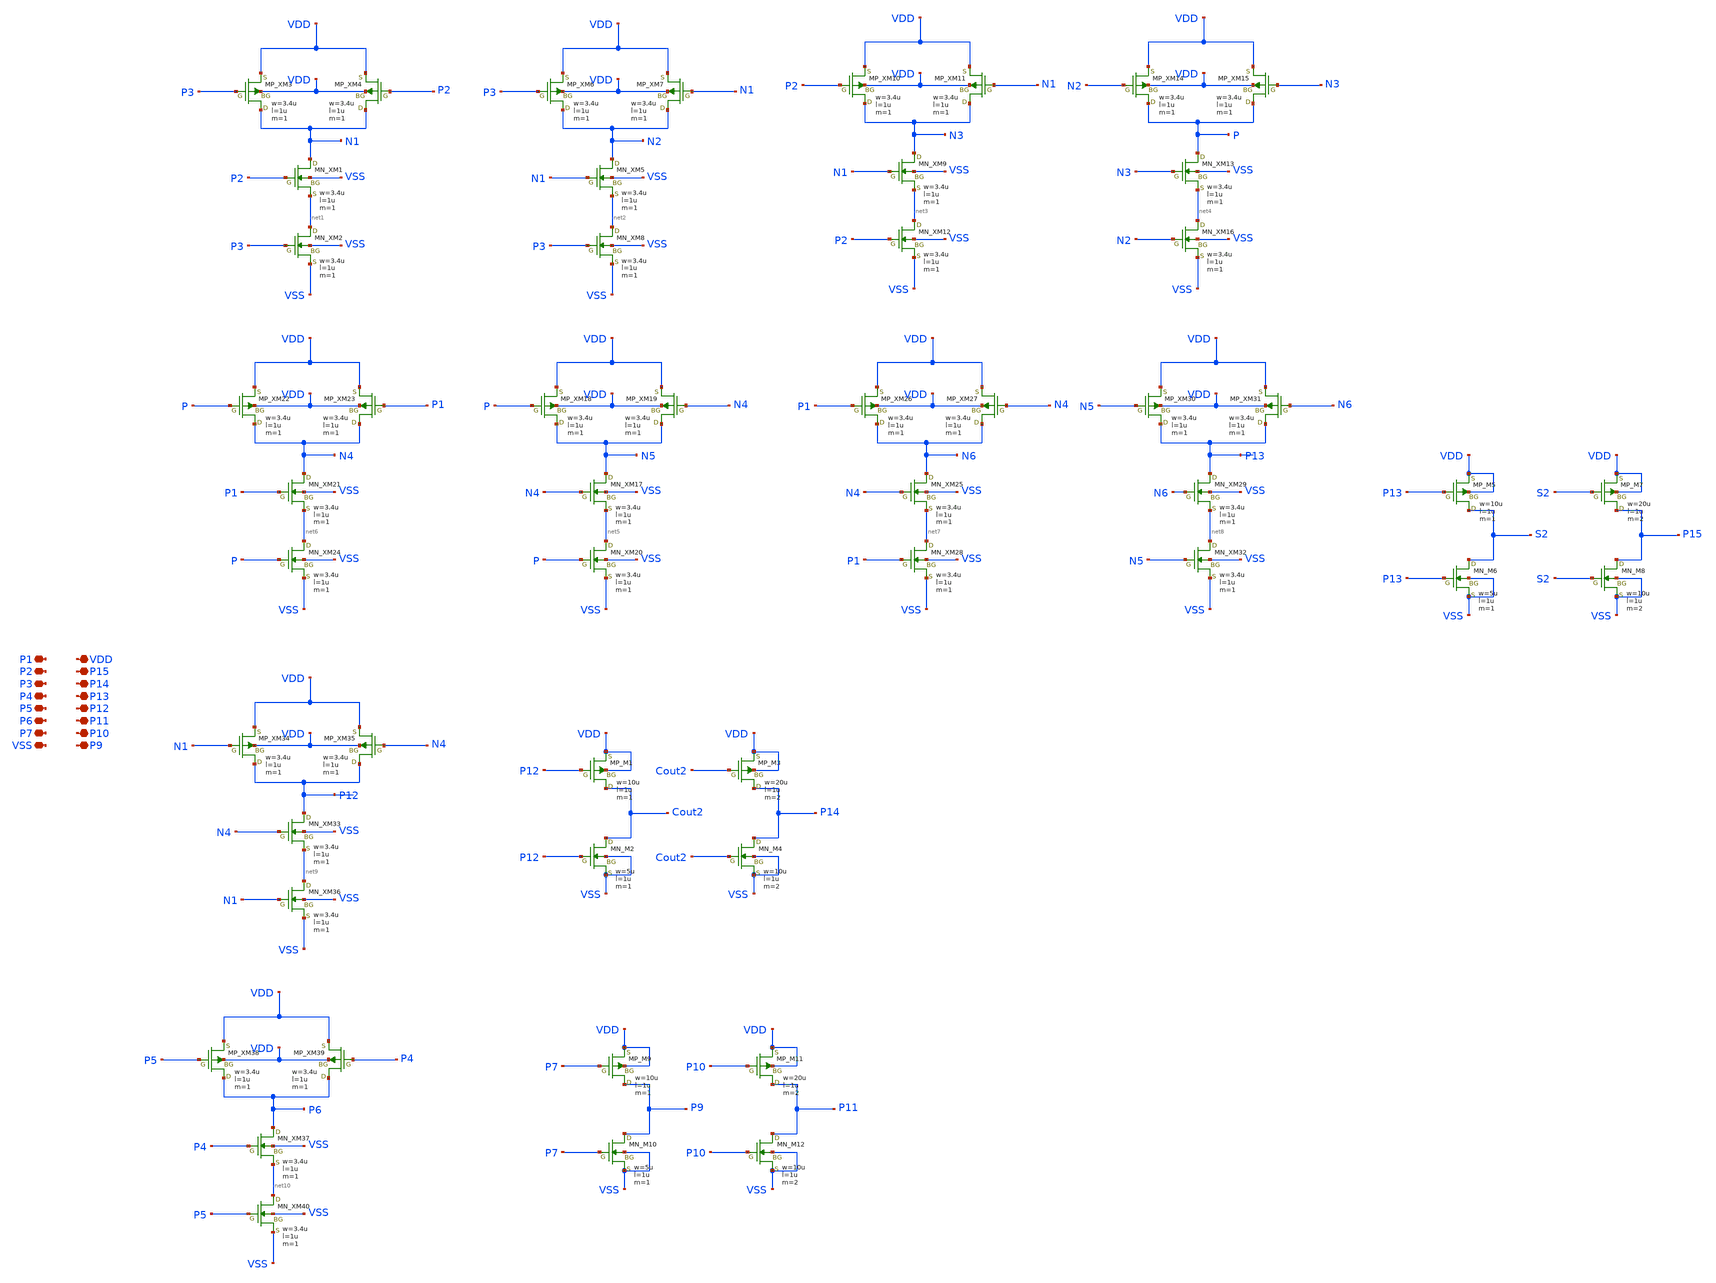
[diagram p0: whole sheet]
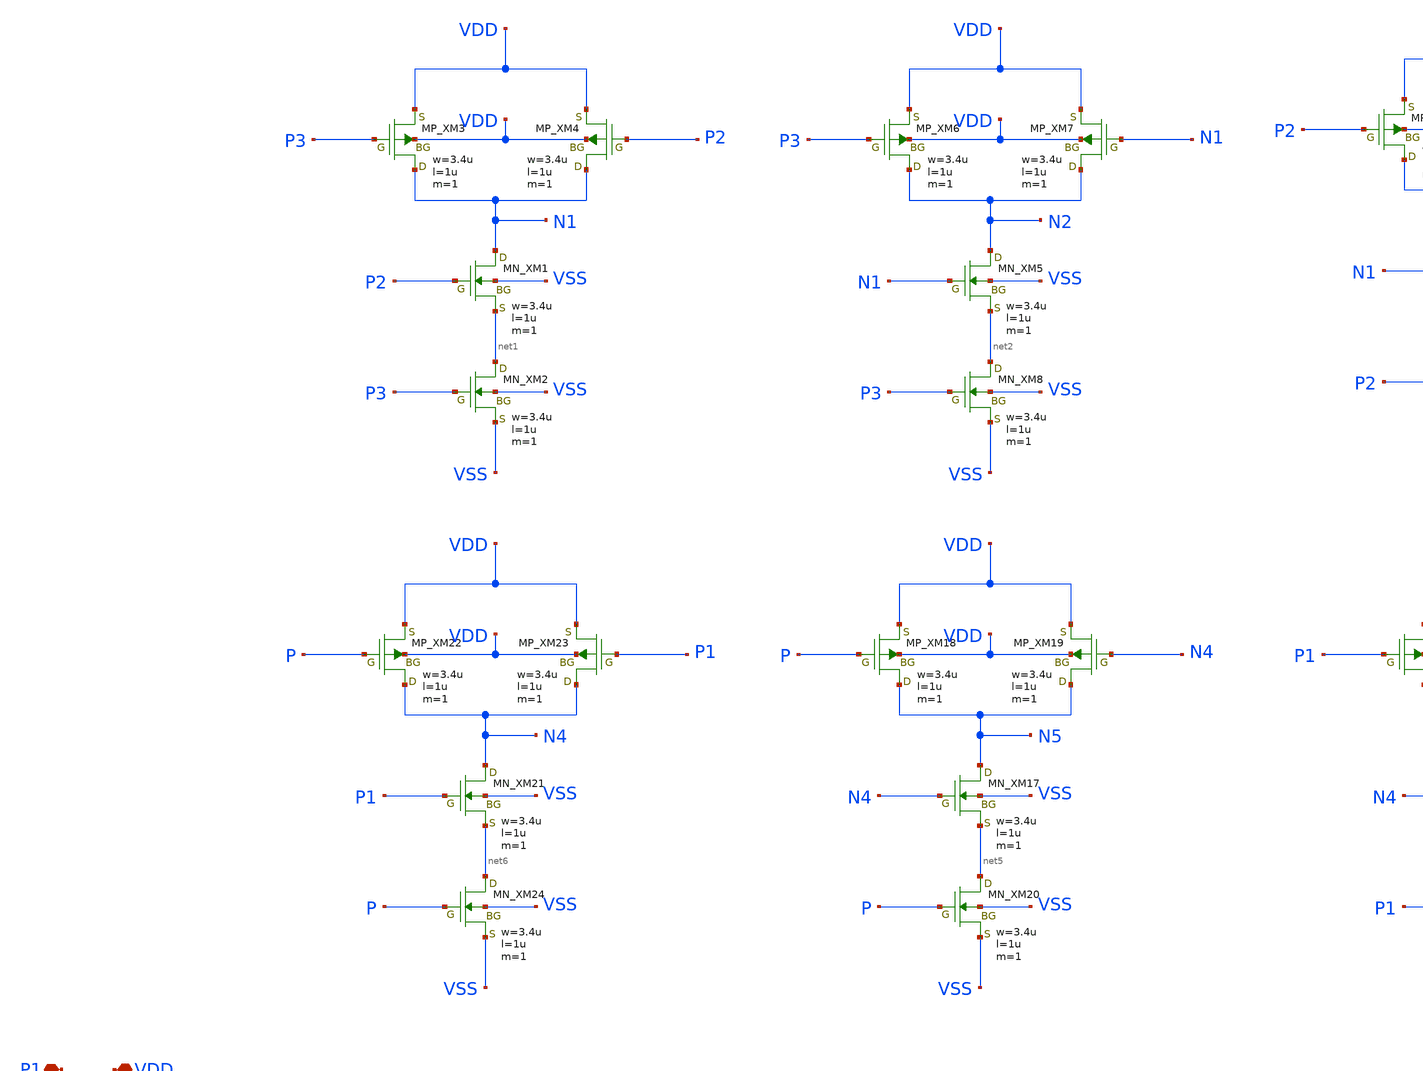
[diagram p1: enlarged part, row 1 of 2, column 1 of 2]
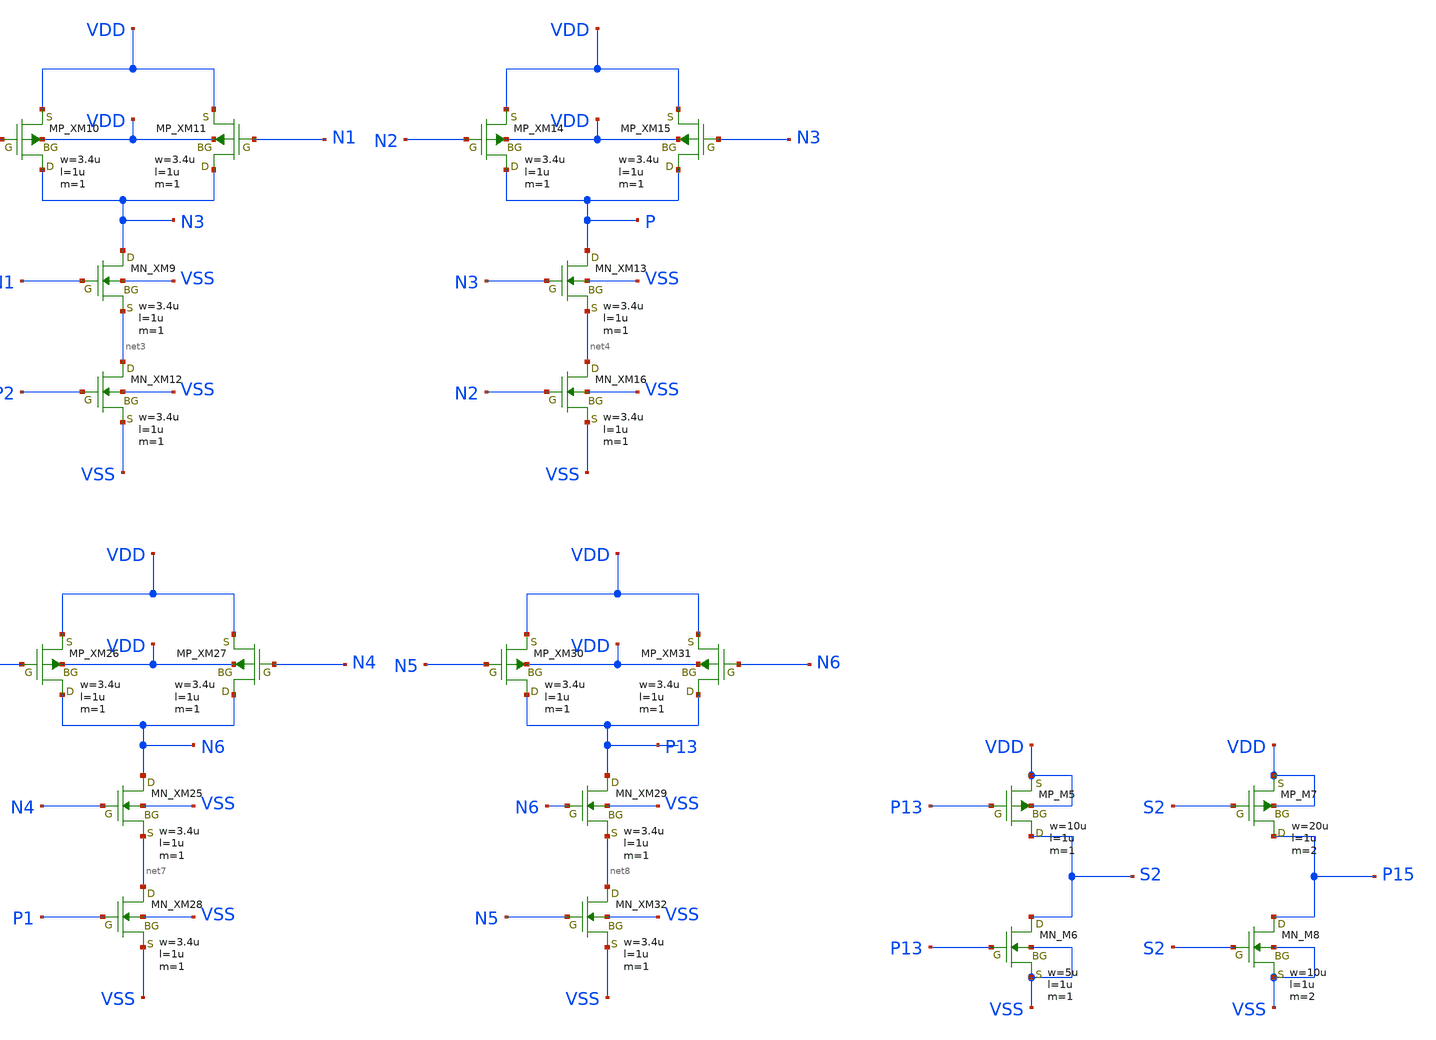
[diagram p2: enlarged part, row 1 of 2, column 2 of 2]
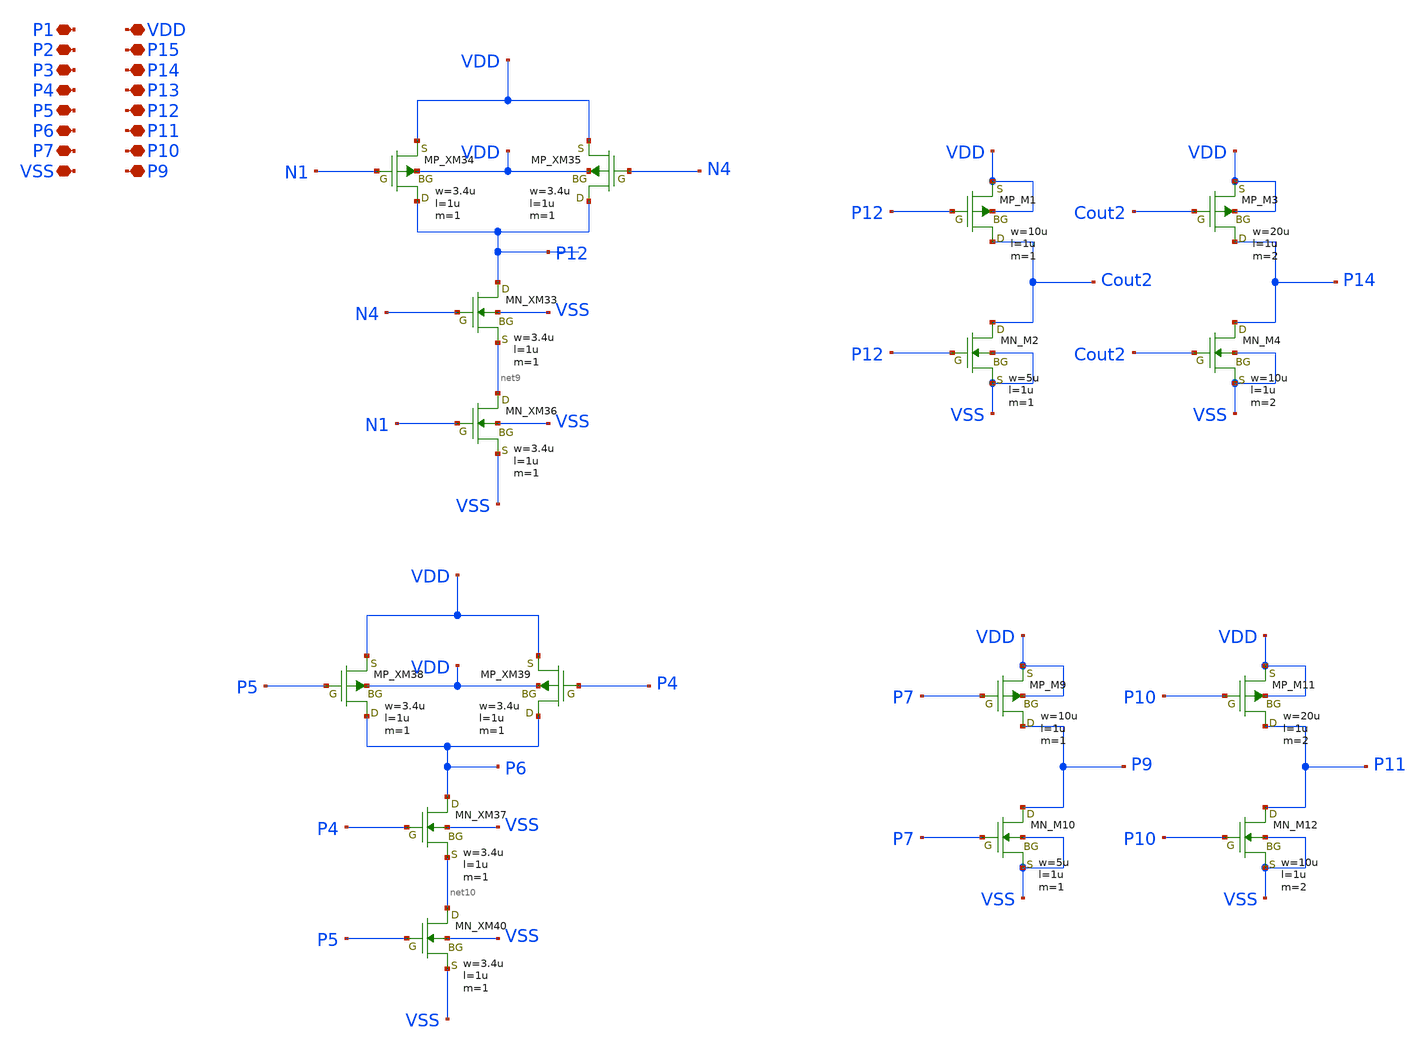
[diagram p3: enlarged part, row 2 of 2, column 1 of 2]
** sch_path: src/tr_1um_AriyoshiNaoki1016jp_bufferadd_ver2.sch
**.subckt tr_1um_AriyoshiNaoki1016jp_bufferadd_ver2 P1 P2 P3 P4 P5 P6 P7 VSS VDD P15 P14 P13 P12 P11
*+ P10 P9
*.iopin P1
*.iopin P2
*.iopin P3
*.iopin P4
*.iopin P5
*.iopin P6
*.iopin P7
*.iopin VSS
*.iopin VDD
*.iopin P15
*.iopin P14
*.iopin P13
*.iopin P12
*.iopin P11
*.iopin P10
*.iopin P9
XXM1 N1 P2 net1 VSS NMOS w=3.4u l=1u nrd=0 nrs=0 m=1
XXM3 N1 P3 VDD VDD PMOS w=3.4u l=1u nrd=0 nrs=0 m=1
XXM4 N1 P2 VDD VDD PMOS w=3.4u l=1u nrd=0 nrs=0 m=1
XXM2 net1 P3 VSS VSS NMOS w=3.4u l=1u nrd=0 nrs=0 m=1
XXM5 N2 N1 net2 VSS NMOS w=3.4u l=1u nrd=0 nrs=0 m=1
XXM6 N2 P3 VDD VDD PMOS w=3.4u l=1u nrd=0 nrs=0 m=1
XXM7 N2 N1 VDD VDD PMOS w=3.4u l=1u nrd=0 nrs=0 m=1
XXM8 net2 P3 VSS VSS NMOS w=3.4u l=1u nrd=0 nrs=0 m=1
XXM9 N3 N1 net3 VSS NMOS w=3.4u l=1u nrd=0 nrs=0 m=1
XXM10 N3 P2 VDD VDD PMOS w=3.4u l=1u nrd=0 nrs=0 m=1
XXM11 N3 N1 VDD VDD PMOS w=3.4u l=1u nrd=0 nrs=0 m=1
XXM12 net3 P2 VSS VSS NMOS w=3.4u l=1u nrd=0 nrs=0 m=1
XXM13 P N3 net4 VSS NMOS w=3.4u l=1u nrd=0 nrs=0 m=1
XXM14 P N2 VDD VDD PMOS w=3.4u l=1u nrd=0 nrs=0 m=1
XXM15 P N3 VDD VDD PMOS w=3.4u l=1u nrd=0 nrs=0 m=1
XXM16 net4 N2 VSS VSS NMOS w=3.4u l=1u nrd=0 nrs=0 m=1
XXM17 N5 N4 net5 VSS NMOS w=3.4u l=1u nrd=0 nrs=0 m=1
XXM18 N5 P VDD VDD PMOS w=3.4u l=1u nrd=0 nrs=0 m=1
XXM19 N5 N4 VDD VDD PMOS w=3.4u l=1u nrd=0 nrs=0 m=1
XXM20 net5 P VSS VSS NMOS w=3.4u l=1u nrd=0 nrs=0 m=1
XXM21 N4 P1 net6 VSS NMOS w=3.4u l=1u nrd=0 nrs=0 m=1
XXM22 N4 P VDD VDD PMOS w=3.4u l=1u nrd=0 nrs=0 m=1
XXM23 N4 P1 VDD VDD PMOS w=3.4u l=1u nrd=0 nrs=0 m=1
XXM24 net6 P VSS VSS NMOS w=3.4u l=1u nrd=0 nrs=0 m=1
XXM25 N6 N4 net7 VSS NMOS w=3.4u l=1u nrd=0 nrs=0 m=1
XXM26 N6 P1 VDD VDD PMOS w=3.4u l=1u nrd=0 nrs=0 m=1
XXM27 N6 N4 VDD VDD PMOS w=3.4u l=1u nrd=0 nrs=0 m=1
XXM28 net7 P1 VSS VSS NMOS w=3.4u l=1u nrd=0 nrs=0 m=1
XXM29 P13 N6 net8 VSS NMOS w=3.4u l=1u nrd=0 nrs=0 m=1
XXM30 P13 N5 VDD VDD PMOS w=3.4u l=1u nrd=0 nrs=0 m=1
XXM31 P13 N6 VDD VDD PMOS w=3.4u l=1u nrd=0 nrs=0 m=1
XXM32 net8 N5 VSS VSS NMOS w=3.4u l=1u nrd=0 nrs=0 m=1
XXM33 P12 N4 net9 VSS NMOS w=3.4u l=1u nrd=0 nrs=0 m=1
XXM34 P12 N1 VDD VDD PMOS w=3.4u l=1u nrd=0 nrs=0 m=1
XXM35 P12 N4 VDD VDD PMOS w=3.4u l=1u nrd=0 nrs=0 m=1
XXM36 net9 N1 VSS VSS NMOS w=3.4u l=1u nrd=0 nrs=0 m=1
XM1 Cout2 P12 VDD VDD PMOS w=10u l=1u nrd=0 nrs=0 m=1
XM2 Cout2 P12 VSS VSS NMOS w=5u l=1u nrd=0 nrs=0 m=1
XM3 P14 Cout2 VDD VDD PMOS w=20u l=1u nrd=0 nrs=0 m=2
XM4 P14 Cout2 VSS VSS NMOS w=10u l=1u nrd=0 nrs=0 m=2
XM5 S2 P13 VDD VDD PMOS w=10u l=1u nrd=0 nrs=0 m=1
XM6 S2 P13 VSS VSS NMOS w=5u l=1u nrd=0 nrs=0 m=1
XM7 P15 S2 VDD VDD PMOS w=20u l=1u nrd=0 nrs=0 m=2
XM8 P15 S2 VSS VSS NMOS w=10u l=1u nrd=0 nrs=0 m=2
XXM37 P6 P4 net10 VSS NMOS w=3.4u l=1u nrd=0 nrs=0 m=1
XXM38 P6 P5 VDD VDD PMOS w=3.4u l=1u nrd=0 nrs=0 m=1
XXM39 P6 P4 VDD VDD PMOS w=3.4u l=1u nrd=0 nrs=0 m=1
XXM40 net10 P5 VSS VSS NMOS w=3.4u l=1u nrd=0 nrs=0 m=1
XM9 P9 P7 VDD VDD PMOS w=10u l=1u nrd=0 nrs=0 m=1
XM10 P9 P7 VSS VSS NMOS w=5u l=1u nrd=0 nrs=0 m=1
XM11 P11 P10 VDD VDD PMOS w=20u l=1u nrd=0 nrs=0 m=2
XM12 P11 P10 VSS VSS NMOS w=10u l=1u nrd=0 nrs=0 m=2
**** begin user architecture code

.include /home/naoki/pdk/TR-1um/libs.tech/spice/models/ip62_models

**** end user architecture code
**.ends
.end
